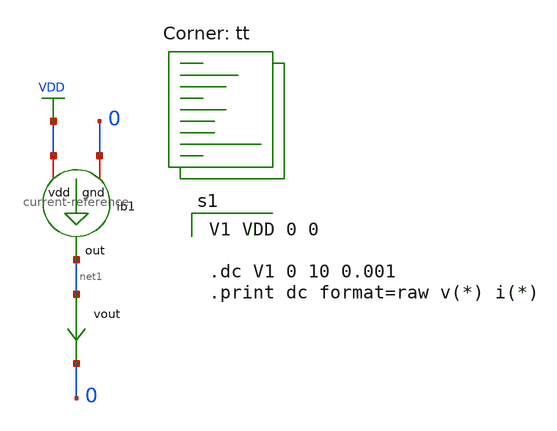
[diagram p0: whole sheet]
** sch_path: charge-pump-2/current-reference-test.sch
**.subckt current-reference-test
ib1 VDD net1 0 current-reference
vout net1 0 0
.save i(vout)
**** begin user architecture code

V1 VDD 0 0

.dc V1 0 10 0.001
.print dc format=raw v(*) i(*)


.lib $::SKYWATER_MODELS/sky130.lib.spice tt
**** end user architecture code
**.ends

* expanding   symbol:
*+  /home/kenrendell/Playground/phase-locked-loop/charge-pump-2/current-reference.sym # of pins=3
** sym_path: charge-pump-2/current-reference.sym
** sch_path: charge-pump-2/current-reference.sch
.subckt current-reference vdd out gnd
*.iopin vdd
*.iopin gnd
*.opin out
XM1 net2 net1 vdd vdd sky130_fd_pr__pfet_01v8 L=2 W=20 nf=1 ad='int((nf+1)/2) * W/nf * 0.29' as='int((nf+2)/2) * W/nf * 0.29'
+ pd='2*int((nf+1)/2) * (W/nf + 0.29)' ps='2*int((nf+2)/2) * (W/nf + 0.29)' nrd='0.29 / W' nrs='0.29 / W'
+ sa=0 sb=0 sd=0 mult=1 m=1
XM2 net1 net7 vdd vdd sky130_fd_pr__pfet_01v8 L=2 W=10 nf=1 ad='int((nf+1)/2) * W/nf * 0.29' as='int((nf+2)/2) * W/nf * 0.29'
+ pd='2*int((nf+1)/2) * (W/nf + 0.29)' ps='2*int((nf+2)/2) * (W/nf + 0.29)' nrd='0.29 / W' nrs='0.29 / W'
+ sa=0 sb=0 sd=0 mult=1 m=1
XM3 net8 net1 vdd vdd sky130_fd_pr__pfet_01v8 L=2 W=16 nf=1 ad='int((nf+1)/2) * W/nf * 0.29' as='int((nf+2)/2) * W/nf * 0.29'
+ pd='2*int((nf+1)/2) * (W/nf + 0.29)' ps='2*int((nf+2)/2) * (W/nf + 0.29)' nrd='0.29 / W' nrs='0.29 / W'
+ sa=0 sb=0 sd=0 mult=1 m=1
XM4 net8 net8 vdd vdd sky130_fd_pr__pfet_01v8 L=2 W=16 nf=1 ad='int((nf+1)/2) * W/nf * 0.29' as='int((nf+2)/2) * W/nf * 0.29'
+ pd='2*int((nf+1)/2) * (W/nf + 0.29)' ps='2*int((nf+2)/2) * (W/nf + 0.29)' nrd='0.29 / W' nrs='0.29 / W'
+ sa=0 sb=0 sd=0 mult=1 m=1
XM5 out net8 vdd vdd sky130_fd_pr__pfet_01v8 L=2 W=200 nf=1 ad='int((nf+1)/2) * W/nf * 0.29' as='int((nf+2)/2) * W/nf * 0.29'
+ pd='2*int((nf+1)/2) * (W/nf + 0.29)' ps='2*int((nf+2)/2) * (W/nf + 0.29)' nrd='0.29 / W' nrs='0.29 / W'
+ sa=0 sb=0 sd=0 mult=1 m=1
R1 net7 net1 sky130_fd_pr__res_generic_m1 W=0.5 L=16000 m=1
R2 net6 net2 sky130_fd_pr__res_generic_m1 W=0.5 L=32000 m=1
XM6 net7 net6 gnd gnd sky130_fd_pr__nfet_01v8 L=2 W=80 nf=1 ad='int((nf+1)/2) * W/nf * 0.29' as='int((nf+2)/2) * W/nf * 0.29'
+ pd='2*int((nf+1)/2) * (W/nf + 0.29)' ps='2*int((nf+2)/2) * (W/nf + 0.29)' nrd='0.29 / W' nrs='0.29 / W'
+ sa=0 sb=0 sd=0 mult=1 m=1
XM7 net6 net2 gnd gnd sky130_fd_pr__nfet_01v8 L=2 W=10 nf=1 ad='int((nf+1)/2) * W/nf * 0.29' as='int((nf+2)/2) * W/nf * 0.29'
+ pd='2*int((nf+1)/2) * (W/nf + 0.29)' ps='2*int((nf+2)/2) * (W/nf + 0.29)' nrd='0.29 / W' nrs='0.29 / W'
+ sa=0 sb=0 sd=0 mult=1 m=1
XM8 net8 net8 net5 net5 sky130_fd_pr__nfet_01v8 L=2 W=100 nf=1 ad='int((nf+1)/2) * W/nf * 0.29' as='int((nf+2)/2) * W/nf * 0.29'
+ pd='2*int((nf+1)/2) * (W/nf + 0.29)' ps='2*int((nf+2)/2) * (W/nf + 0.29)' nrd='0.29 / W' nrs='0.29 / W'
+ sa=0 sb=0 sd=0 mult=1 m=1
XM9 net5 net6 gnd gnd sky130_fd_pr__nfet_01v8 L=2 W=100 nf=1 ad='int((nf+1)/2) * W/nf * 0.29' as='int((nf+2)/2) * W/nf * 0.29'
+ pd='2*int((nf+1)/2) * (W/nf + 0.29)' ps='2*int((nf+2)/2) * (W/nf + 0.29)' nrd='0.29 / W' nrs='0.29 / W'
+ sa=0 sb=0 sd=0 mult=1 m=1
XM10 net1 net4 gnd gnd sky130_fd_pr__nfet_01v8 L=2 W=10 nf=1 ad='int((nf+1)/2) * W/nf * 0.29' as='int((nf+2)/2) * W/nf * 0.29'
+ pd='2*int((nf+1)/2) * (W/nf + 0.29)' ps='2*int((nf+2)/2) * (W/nf + 0.29)' nrd='0.29 / W' nrs='0.29 / W'
+ sa=0 sb=0 sd=0 mult=1 m=1
XM11 net4 net3 gnd gnd sky130_fd_pr__nfet_01v8 L=2 W=10 nf=1 ad='int((nf+1)/2) * W/nf * 0.29' as='int((nf+2)/2) * W/nf * 0.29'
+ pd='2*int((nf+1)/2) * (W/nf + 0.29)' ps='2*int((nf+2)/2) * (W/nf + 0.29)' nrd='0.29 / W' nrs='0.29 / W'
+ sa=0 sb=0 sd=0 mult=1 m=1
R3 net4 net3 sky130_fd_pr__res_generic_m1 W=0.5 L=12000 m=1
R4 net3 vdd sky130_fd_pr__res_generic_m1 W=0.5 L=80000 m=1
.ends

.GLOBAL VDD
.end
